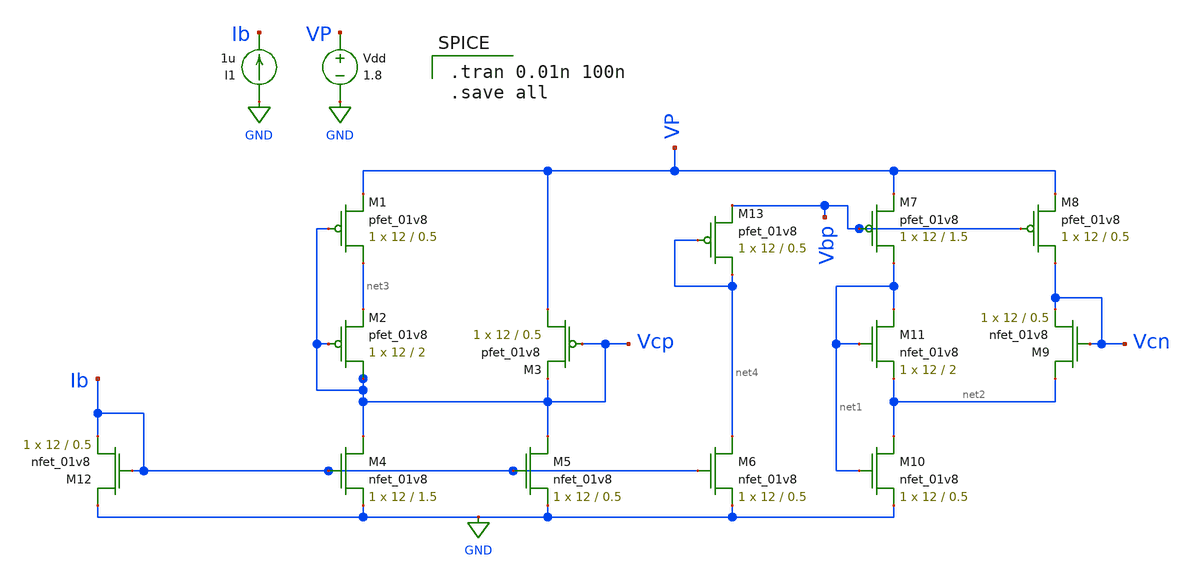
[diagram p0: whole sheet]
** sch_path: mp3/schematic/bias_circuit.sch
**.subckt bias_circuit
XM1 net3 Vcp VP VDD sky130_fd_pr__pfet_01v8 L=0.5 W=12 nf=1 ad='int((nf+1)/2) * W/nf * 0.29' as='int((nf+2)/2) * W/nf * 0.29'
+ pd='2*int((nf+1)/2) * (W/nf + 0.29)' ps='2*int((nf+2)/2) * (W/nf + 0.29)' nrd='0.29 / W' nrs='0.29 / W'
+ sa=0 sb=0 sd=0 mult=1 m=1
XM2 Vcp Vcp net3 VDD sky130_fd_pr__pfet_01v8 L=2 W=12 nf=1 ad='int((nf+1)/2) * W/nf * 0.29' as='int((nf+2)/2) * W/nf * 0.29'
+ pd='2*int((nf+1)/2) * (W/nf + 0.29)' ps='2*int((nf+2)/2) * (W/nf + 0.29)' nrd='0.29 / W' nrs='0.29 / W'
+ sa=0 sb=0 sd=0 mult=1 m=1
XM3 VP Vcp Vcp VDD sky130_fd_pr__pfet_01v8 L=0.5 W=12 nf=1 ad='int((nf+1)/2) * W/nf * 0.29' as='int((nf+2)/2) * W/nf * 0.29'
+ pd='2*int((nf+1)/2) * (W/nf + 0.29)' ps='2*int((nf+2)/2) * (W/nf + 0.29)' nrd='0.29 / W' nrs='0.29 / W'
+ sa=0 sb=0 sd=0 mult=1 m=1
XM4 Vcp Ib GND GND sky130_fd_pr__nfet_01v8 L=1.5 W=12 nf=1 ad='int((nf+1)/2) * W/nf * 0.29' as='int((nf+2)/2) * W/nf * 0.29'
+ pd='2*int((nf+1)/2) * (W/nf + 0.29)' ps='2*int((nf+2)/2) * (W/nf + 0.29)' nrd='0.29 / W' nrs='0.29 / W'
+ sa=0 sb=0 sd=0 mult=1 m=1
XM5 Vcp Ib GND GND sky130_fd_pr__nfet_01v8 L=0.5 W=12 nf=1 ad='int((nf+1)/2) * W/nf * 0.29' as='int((nf+2)/2) * W/nf * 0.29'
+ pd='2*int((nf+1)/2) * (W/nf + 0.29)' ps='2*int((nf+2)/2) * (W/nf + 0.29)' nrd='0.29 / W' nrs='0.29 / W'
+ sa=0 sb=0 sd=0 mult=1 m=1
XM6 net4 Ib GND GND sky130_fd_pr__nfet_01v8 L=0.5 W=12 nf=1 ad='int((nf+1)/2) * W/nf * 0.29' as='int((nf+2)/2) * W/nf * 0.29'
+ pd='2*int((nf+1)/2) * (W/nf + 0.29)' ps='2*int((nf+2)/2) * (W/nf + 0.29)' nrd='0.29 / W' nrs='0.29 / W'
+ sa=0 sb=0 sd=0 mult=1 m=1
XM7 net1 Vbp VP VDD sky130_fd_pr__pfet_01v8 L=1.5 W=12 nf=1 ad='int((nf+1)/2) * W/nf * 0.29' as='int((nf+2)/2) * W/nf * 0.29'
+ pd='2*int((nf+1)/2) * (W/nf + 0.29)' ps='2*int((nf+2)/2) * (W/nf + 0.29)' nrd='0.29 / W' nrs='0.29 / W'
+ sa=0 sb=0 sd=0 mult=1 m=1
XM8 Vcn Vbp VP VDD sky130_fd_pr__pfet_01v8 L=0.5 W=12 nf=1 ad='int((nf+1)/2) * W/nf * 0.29' as='int((nf+2)/2) * W/nf * 0.29'
+ pd='2*int((nf+1)/2) * (W/nf + 0.29)' ps='2*int((nf+2)/2) * (W/nf + 0.29)' nrd='0.29 / W' nrs='0.29 / W'
+ sa=0 sb=0 sd=0 mult=1 m=1
XM9 net2 Vcn Vcn GND sky130_fd_pr__nfet_01v8 L=0.5 W=12 nf=1 ad='int((nf+1)/2) * W/nf * 0.29' as='int((nf+2)/2) * W/nf * 0.29'
+ pd='2*int((nf+1)/2) * (W/nf + 0.29)' ps='2*int((nf+2)/2) * (W/nf + 0.29)' nrd='0.29 / W' nrs='0.29 / W'
+ sa=0 sb=0 sd=0 mult=1 m=1
XM10 net2 net1 GND GND sky130_fd_pr__nfet_01v8 L=0.5 W=12 nf=1 ad='int((nf+1)/2) * W/nf * 0.29' as='int((nf+2)/2) * W/nf * 0.29'
+ pd='2*int((nf+1)/2) * (W/nf + 0.29)' ps='2*int((nf+2)/2) * (W/nf + 0.29)' nrd='0.29 / W' nrs='0.29 / W'
+ sa=0 sb=0 sd=0 mult=1 m=1
XM11 net1 net1 net2 GND sky130_fd_pr__nfet_01v8 L=2 W=12 nf=1 ad='int((nf+1)/2) * W/nf * 0.29' as='int((nf+2)/2) * W/nf * 0.29'
+ pd='2*int((nf+1)/2) * (W/nf + 0.29)' ps='2*int((nf+2)/2) * (W/nf + 0.29)' nrd='0.29 / W' nrs='0.29 / W'
+ sa=0 sb=0 sd=0 mult=1 m=1
I1 GND Ib 1u
XM12 GND Ib Ib GND sky130_fd_pr__nfet_01v8 L=0.5 W=12 nf=1 ad='int((nf+1)/2) * W/nf * 0.29' as='int((nf+2)/2) * W/nf * 0.29'
+ pd='2*int((nf+1)/2) * (W/nf + 0.29)' ps='2*int((nf+2)/2) * (W/nf + 0.29)' nrd='0.29 / W' nrs='0.29 / W'
+ sa=0 sb=0 sd=0 mult=1 m=1
Vdd VP GND 1.8
XM13 net4 net4 Vbp VDD sky130_fd_pr__pfet_01v8 L=0.5 W=12 nf=1 ad='int((nf+1)/2) * W/nf * 0.29' as='int((nf+2)/2) * W/nf * 0.29'
+ pd='2*int((nf+1)/2) * (W/nf + 0.29)' ps='2*int((nf+2)/2) * (W/nf + 0.29)' nrd='0.29 / W' nrs='0.29 / W'
+ sa=0 sb=0 sd=0 mult=1 m=1
**** begin user architecture code

.option wnflag=1
.lib ~/skywater/skywater-pdk/libraries/sky130_fd_pr_ngspice/latest/models/sky130.lib.spice tt


.tran 0.01n 100n
.save all

**** end user architecture code
**.ends
.GLOBAL GND
.end
